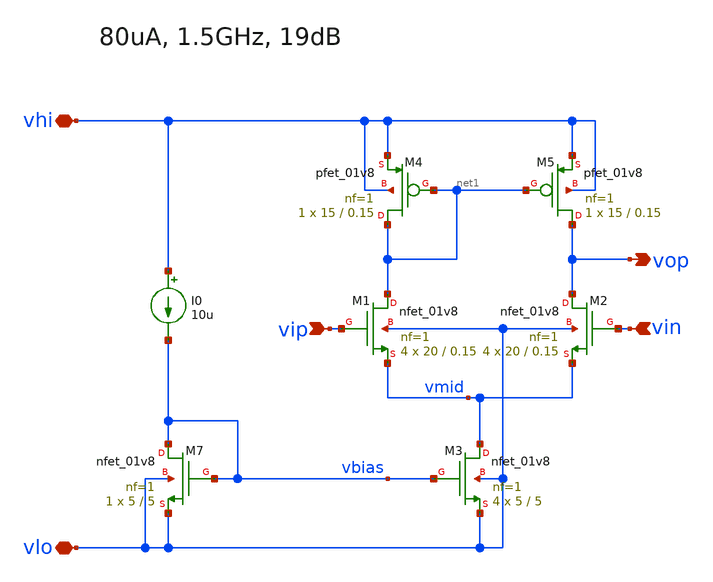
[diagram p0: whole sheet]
** sch_path: xschem/5tamp_model.sch
**.subckt 5tamp_model vip vin vop vhi vlo
*.ipin vip
*.ipin vin
*.opin vop
*.iopin vhi
*.iopin vlo
XM1 net1 vip vmid vlo sky130_fd_pr__nfet_01v8 L=0.15 W=20 nf=1 ad='int((nf+1)/2) * W/nf * 0.29' as='int((nf+2)/2) * W/nf * 0.29'
+ pd='2*int((nf+1)/2) * (W/nf + 0.29)' ps='2*int((nf+2)/2) * (W/nf + 0.29)' nrd='0.29 / W' nrs='0.29 / W'
+ sa=0 sb=0 sd=0 mult=4 m=4
XM2 vop vin vmid vlo sky130_fd_pr__nfet_01v8 L=0.15 W=20 nf=1 ad='int((nf+1)/2) * W/nf * 0.29' as='int((nf+2)/2) * W/nf * 0.29'
+ pd='2*int((nf+1)/2) * (W/nf + 0.29)' ps='2*int((nf+2)/2) * (W/nf + 0.29)' nrd='0.29 / W' nrs='0.29 / W'
+ sa=0 sb=0 sd=0 mult=4 m=4
XM3 vmid vbias vlo vlo sky130_fd_pr__nfet_01v8 L=5 W=5 nf=1 ad='int((nf+1)/2) * W/nf * 0.29' as='int((nf+2)/2) * W/nf * 0.29'
+ pd='2*int((nf+1)/2) * (W/nf + 0.29)' ps='2*int((nf+2)/2) * (W/nf + 0.29)' nrd='0.29 / W' nrs='0.29 / W'
+ sa=0 sb=0 sd=0 mult=4 m=4
XM4 net1 net1 vhi vhi sky130_fd_pr__pfet_01v8 L=0.15 W=15 nf=1 ad='int((nf+1)/2) * W/nf * 0.29' as='int((nf+2)/2) * W/nf * 0.29'
+ pd='2*int((nf+1)/2) * (W/nf + 0.29)' ps='2*int((nf+2)/2) * (W/nf + 0.29)' nrd='0.29 / W' nrs='0.29 / W'
+ sa=0 sb=0 sd=0 mult=1 m=1
XM5 vop net1 vhi vhi sky130_fd_pr__pfet_01v8 L=0.15 W=15 nf=1 ad='int((nf+1)/2) * W/nf * 0.29' as='int((nf+2)/2) * W/nf * 0.29'
+ pd='2*int((nf+1)/2) * (W/nf + 0.29)' ps='2*int((nf+2)/2) * (W/nf + 0.29)' nrd='0.29 / W' nrs='0.29 / W'
+ sa=0 sb=0 sd=0 mult=1 m=1
I0 vhi vbias 10u
XM7 vbias vbias vlo vlo sky130_fd_pr__nfet_01v8 L=5 W=5 nf=1 ad='int((nf+1)/2) * W/nf * 0.29' as='int((nf+2)/2) * W/nf * 0.29'
+ pd='2*int((nf+1)/2) * (W/nf + 0.29)' ps='2*int((nf+2)/2) * (W/nf + 0.29)' nrd='0.29 / W' nrs='0.29 / W'
+ sa=0 sb=0 sd=0 mult=1 m=1
**.ends
.end
